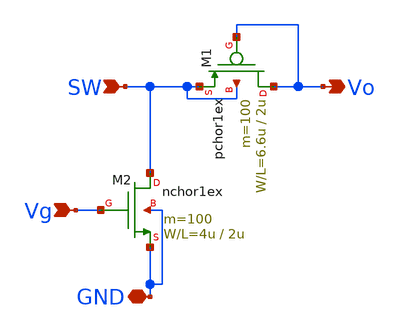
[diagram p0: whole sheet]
** sch_path: design/xschem/BoostDCDC_LVS.sch
**.subckt BoostDCDC_LVS Vo SW Vg GND
*.opin Vo
*.ipin SW
*.ipin Vg
*.iopin GND
M1 Vo Vo SW SW pchor1ex L=2u W=6.6u m=100
M2 SW Vg GND GND nchor1ex L=2u W=4u m=100
**.ends
.end
